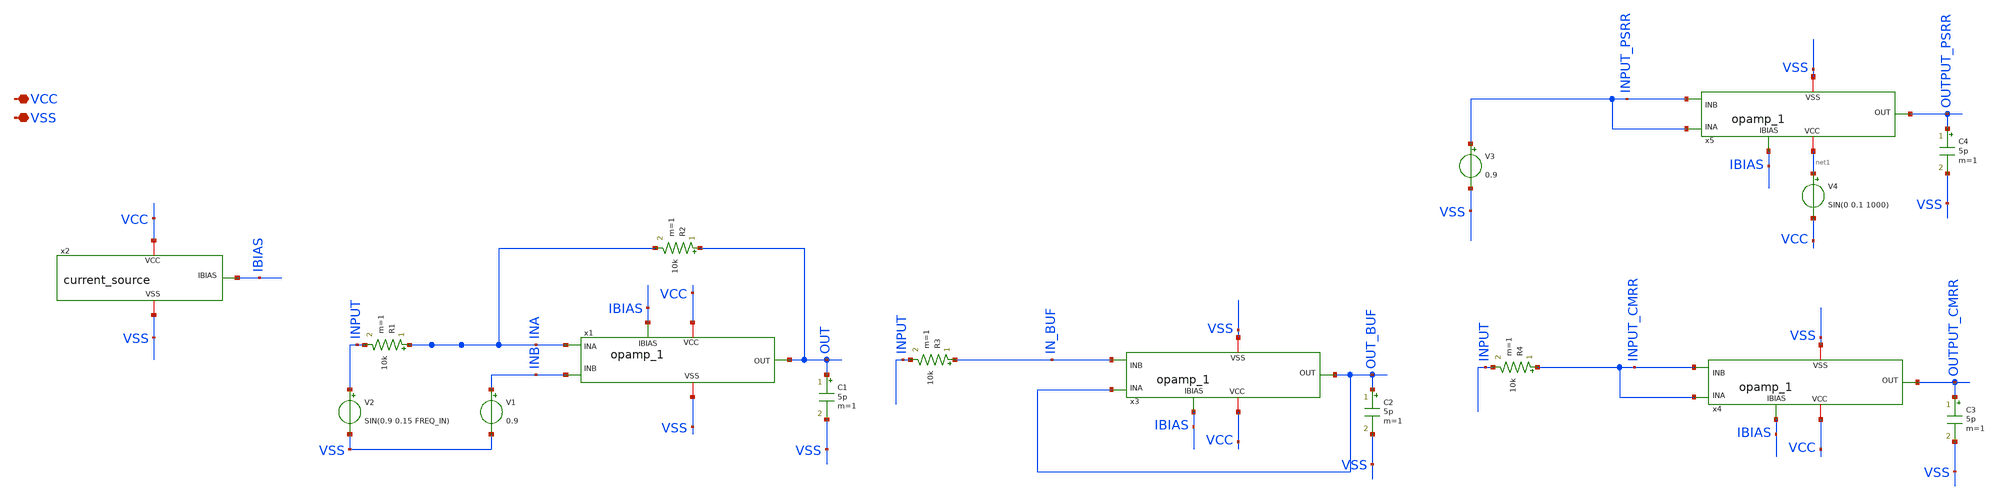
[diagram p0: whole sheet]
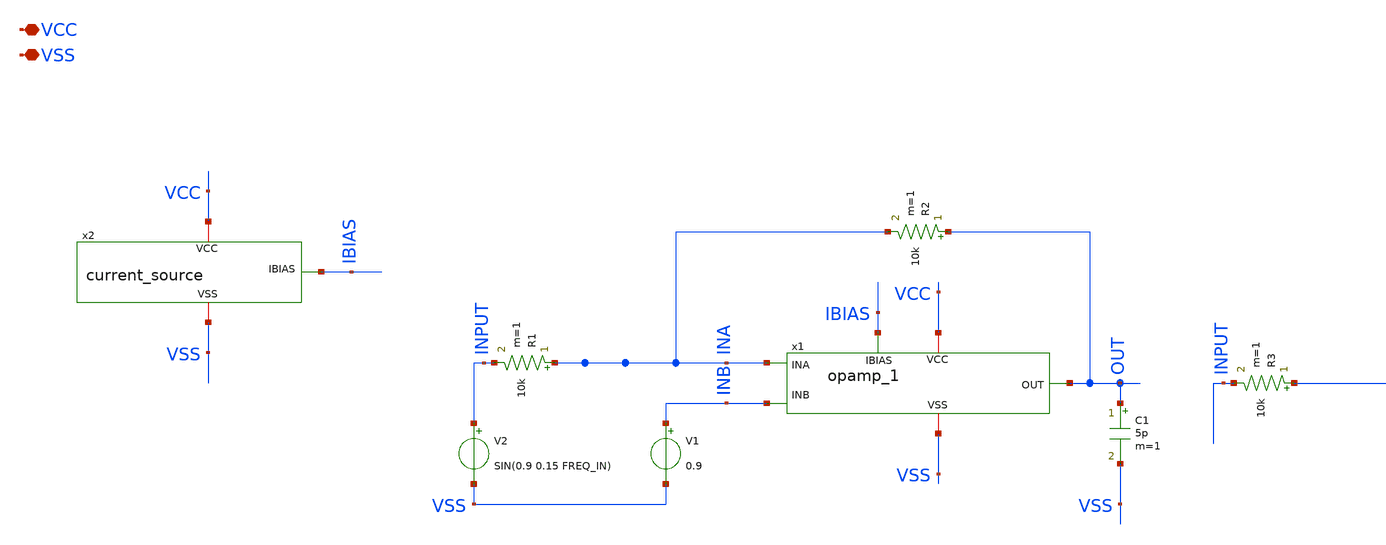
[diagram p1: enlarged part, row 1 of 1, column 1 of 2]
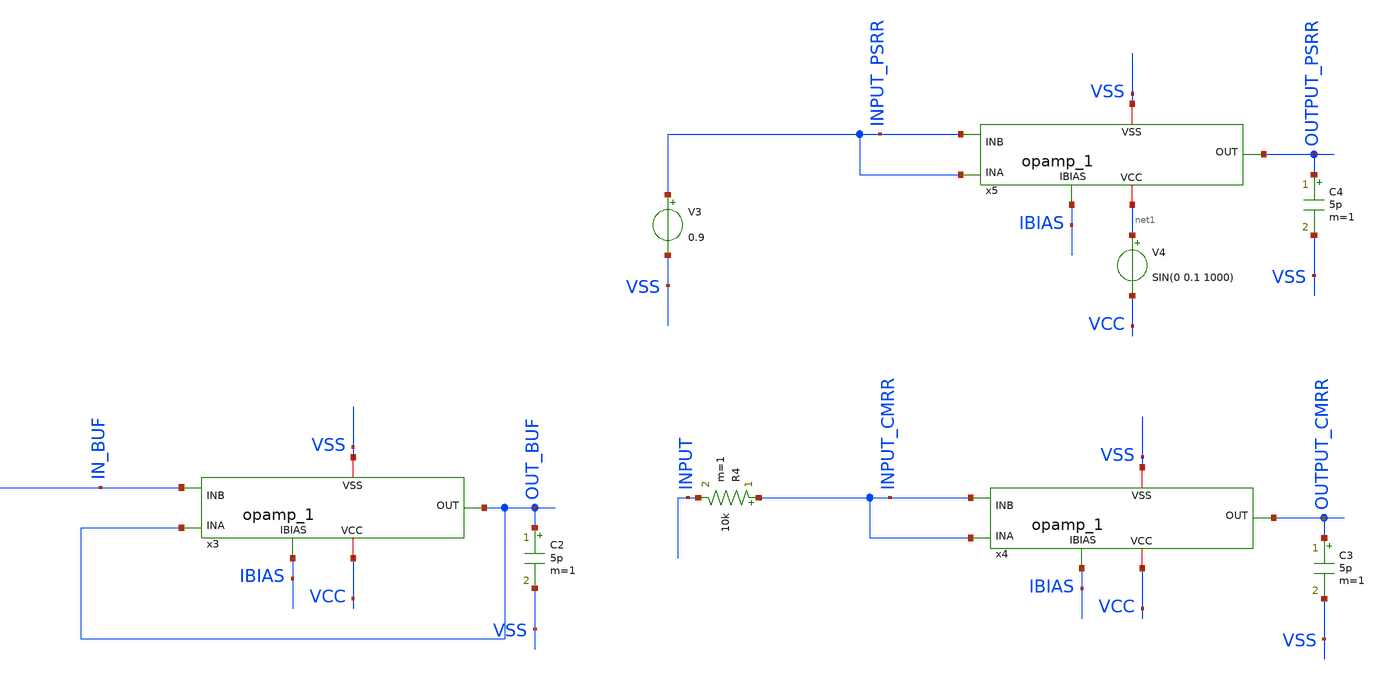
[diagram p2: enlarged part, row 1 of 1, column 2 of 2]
** sch_path: xschem/opamp_1_tb_2.sch
**.subckt opamp_1_tb_2 VCC VSS
*.iopin VCC
*.iopin VSS
x1 VCC OUT INA INB VSS IBIAS opamp_1
V1 INB VSS 0.9
V2 INPUT VSS SIN(0.9 0.15 FREQ_IN)
R1 INA INPUT 10k m=1
R2 OUT INA 10k m=1
C1 OUT VSS 5p m=1
x2 VCC VSS IBIAS current_source
x3 VCC OUT_BUF OUT_BUF IN_BUF VSS IBIAS opamp_1
R3 IN_BUF INPUT 10k m=1
C2 OUT_BUF VSS 5p m=1
x4 VCC OUTPUT_CMRR INPUT_CMRR INPUT_CMRR VSS IBIAS opamp_1
R4 INPUT_CMRR INPUT 10k m=1
C3 OUTPUT_CMRR VSS 5p m=1
x5 net1 OUTPUT_PSRR INPUT_PSRR INPUT_PSRR VSS IBIAS opamp_1
C4 OUTPUT_PSRR VSS 5p m=1
V3 INPUT_PSRR VSS 0.9
V4 net1 VCC SIN(0 0.1 1000)
**** begin user architecture code

** opencircuitdesign pdks install
.lib $::SKYWATER_MODELS/sky130.lib.spice tt





* ngspice commands
.param VCC=1.8
.param FREQ_IN=50000000
vvss vss 0 dc 0
vvcc vcc 0 pwl 0 0 10n 0 10.1n VCC 4000n VCC

.control
tran 100p 4000n
write inverter_tb.raw
.endc




**** end user architecture code
**.ends

* expanding   symbol:  opamp_1.sym # of pins=6
** sym_path: xschem/opamp_1.sym
** sch_path: xschem/opamp_1.sch
.subckt opamp_1 VCC OUT INA INB VSS IBIAS
*.ipin INA
*.ipin INB
*.opin OUT
*.iopin VCC
*.iopin VSS
*.ipin IBIAS
x1 DIFF_OUT MIRR INA INB TAILV VSS indiff
x2 VCC DIFF_OUT MIRR activeload
x3 VCC IBIAS DIFF_OUT RN VSS active-resistor
x4 TAILV IBIAS VSS tail_current
x5 VCC DIFF_OUT OUT IBIAS VSS second_stage
XC2 RN OUT sky130_fd_pr__cap_mim_m3_1 W=20 L=13 MF=1 m=1
.ends


* expanding   symbol:  current_source.sym # of pins=3
** sym_path: xschem/current_source.sym
** sch_path: xschem/current_source.sch
.subckt current_source VCC VSS IBIAS
*.iopin VCC
*.iopin VSS
*.opin IBIAS
XM3 IBIAS IBIAS VSS VSS sky130_fd_pr__nfet_01v8 L=1 W=40 nf=1 ad='int((nf+1)/2) * W/nf * 0.29' as='int((nf+2)/2) * W/nf * 0.29'
+ pd='2*int((nf+1)/2) * (W/nf + 0.29)' ps='2*int((nf+2)/2) * (W/nf + 0.29)' nrd='0.29 / W' nrs='0.29 / W'
+ sa=0 sb=0 sd=0 mult=1 m=1
XR1 IBIAS VCC VSS sky130_fd_pr__res_xhigh_po W=1 L=9 mult=1 m=1
.ends


* expanding   symbol:  indiff.sym # of pins=6
** sym_path: xschem/indiff.sym
** sch_path: xschem/indiff.sch
.subckt indiff DB DA INA INB S VSS
*.ipin INA
*.ipin INB
*.iopin DA
*.iopin DB
*.iopin S
*.iopin VSS
XM1 DA INA S VSS sky130_fd_pr__nfet_01v8 L=1 W=5 nf=1 ad='int((nf+1)/2) * W/nf * 0.29' as='int((nf+2)/2) * W/nf * 0.29'
+ pd='2*int((nf+1)/2) * (W/nf + 0.29)' ps='2*int((nf+2)/2) * (W/nf + 0.29)' nrd='0.29 / W' nrs='0.29 / W'
+ sa=0 sb=0 sd=0 mult=4 m=4
XM2 DB INB S VSS sky130_fd_pr__nfet_01v8 L=1 W=5 nf=1 ad='int((nf+1)/2) * W/nf * 0.29' as='int((nf+2)/2) * W/nf * 0.29'
+ pd='2*int((nf+1)/2) * (W/nf + 0.29)' ps='2*int((nf+2)/2) * (W/nf + 0.29)' nrd='0.29 / W' nrs='0.29 / W'
+ sa=0 sb=0 sd=0 mult=4 m=4
.ends


* expanding   symbol:  activeload.sym # of pins=3
** sym_path: xschem/activeload.sym
** sch_path: xschem/activeload.sch
.subckt activeload VCC DB DA
*.iopin DA
*.iopin DB
*.iopin VCC
XM4 DA DA VCC VCC sky130_fd_pr__pfet_01v8_lvt L=0.5 W=5 nf=1 ad='int((nf+1)/2) * W/nf * 0.29' as='int((nf+2)/2) * W/nf * 0.29'
+ pd='2*int((nf+1)/2) * (W/nf + 0.29)' ps='2*int((nf+2)/2) * (W/nf + 0.29)' nrd='0.29 / W' nrs='0.29 / W'
+ sa=0 sb=0 sd=0 mult=3 m=3
XM5 DB DA VCC VCC sky130_fd_pr__pfet_01v8_lvt L=0.5 W=5 nf=1 ad='int((nf+1)/2) * W/nf * 0.29' as='int((nf+2)/2) * W/nf * 0.29'
+ pd='2*int((nf+1)/2) * (W/nf + 0.29)' ps='2*int((nf+2)/2) * (W/nf + 0.29)' nrd='0.29 / W' nrs='0.29 / W'
+ sa=0 sb=0 sd=0 mult=3 m=3
.ends


* expanding   symbol:  active-resistor.sym # of pins=5
** sym_path: xschem/active-resistor.sym
** sch_path: xschem/active-resistor.sch
.subckt active-resistor VCC IBIAS RP RN VSS
*.iopin VCC
*.iopin VSS
*.ipin IBIAS
*.iopin RP
*.iopin RN
XM9 RBIAS IBIAS VSS VSS sky130_fd_pr__nfet_01v8 L=1 W=5 nf=1 ad='int((nf+1)/2) * W/nf * 0.29' as='int((nf+2)/2) * W/nf * 0.29'
+ pd='2*int((nf+1)/2) * (W/nf + 0.29)' ps='2*int((nf+2)/2) * (W/nf + 0.29)' nrd='0.29 / W' nrs='0.29 / W'
+ sa=0 sb=0 sd=0 mult=1 m=1
XM10 RBIAS RBIAS net1 VCC sky130_fd_pr__pfet_01v8_lvt L=0.5 W=1 nf=1 ad='int((nf+1)/2) * W/nf * 0.29'
+ as='int((nf+2)/2) * W/nf * 0.29' pd='2*int((nf+1)/2) * (W/nf + 0.29)' ps='2*int((nf+2)/2) * (W/nf + 0.29)'
+ nrd='0.29 / W' nrs='0.29 / W' sa=0 sb=0 sd=0 mult=1 m=1
XM11 net1 net1 VCC VCC sky130_fd_pr__pfet_01v8_lvt L=0.5 W=7.5 nf=1 ad='int((nf+1)/2) * W/nf * 0.29'
+ as='int((nf+2)/2) * W/nf * 0.29' pd='2*int((nf+1)/2) * (W/nf + 0.29)' ps='2*int((nf+2)/2) * (W/nf + 0.29)'
+ nrd='0.29 / W' nrs='0.29 / W' sa=0 sb=0 sd=0 mult=1 m=1
XM8 RN RBIAS RP VCC sky130_fd_pr__pfet_01v8_lvt L=0.5 W=7 nf=1 ad='int((nf+1)/2) * W/nf * 0.29' as='int((nf+2)/2) * W/nf * 0.29'
+ pd='2*int((nf+1)/2) * (W/nf + 0.29)' ps='2*int((nf+2)/2) * (W/nf + 0.29)' nrd='0.29 / W' nrs='0.29 / W'
+ sa=0 sb=0 sd=0 mult=2 m=2
.ends


* expanding   symbol:  tail_current.sym # of pins=3
** sym_path: xschem/tail_current.sym
** sch_path: xschem/tail_current.sch
.subckt tail_current TAILV IBIAS VSS
*.iopin VSS
*.ipin IBIAS
*.iopin TAILV
XM3 TAILV IBIAS VSS VSS sky130_fd_pr__nfet_01v8 L=1 W=5 nf=1 ad='int((nf+1)/2) * W/nf * 0.29' as='int((nf+2)/2) * W/nf * 0.29'
+ pd='2*int((nf+1)/2) * (W/nf + 0.29)' ps='2*int((nf+2)/2) * (W/nf + 0.29)' nrd='0.29 / W' nrs='0.29 / W'
+ sa=0 sb=0 sd=0 mult=8 m=8
.ends


* expanding   symbol:  second_stage.sym # of pins=5
** sym_path: xschem/second_stage.sym
** sch_path: xschem/second_stage.sch
.subckt second_stage VCC DIFF_OUT OUT IBIAS VSS
*.iopin VCC
*.iopin VSS
*.ipin IBIAS
*.ipin DIFF_OUT
*.opin OUT
XM6 OUT IBIAS VSS VSS sky130_fd_pr__nfet_01v8 L=0.5 W=5 nf=1 ad='int((nf+1)/2) * W/nf * 0.29' as='int((nf+2)/2) * W/nf * 0.29'
+ pd='2*int((nf+1)/2) * (W/nf + 0.29)' ps='2*int((nf+2)/2) * (W/nf + 0.29)' nrd='0.29 / W' nrs='0.29 / W'
+ sa=0 sb=0 sd=0 mult=19 m=19
XM2 OUT DIFF_OUT VCC VCC sky130_fd_pr__pfet_01v8_lvt L=0.5 W=5 nf=1 ad='int((nf+1)/2) * W/nf * 0.29'
+ as='int((nf+2)/2) * W/nf * 0.29' pd='2*int((nf+1)/2) * (W/nf + 0.29)' ps='2*int((nf+2)/2) * (W/nf + 0.29)'
+ nrd='0.29 / W' nrs='0.29 / W' sa=0 sb=0 sd=0 mult=14 m=14
.ends

.end
